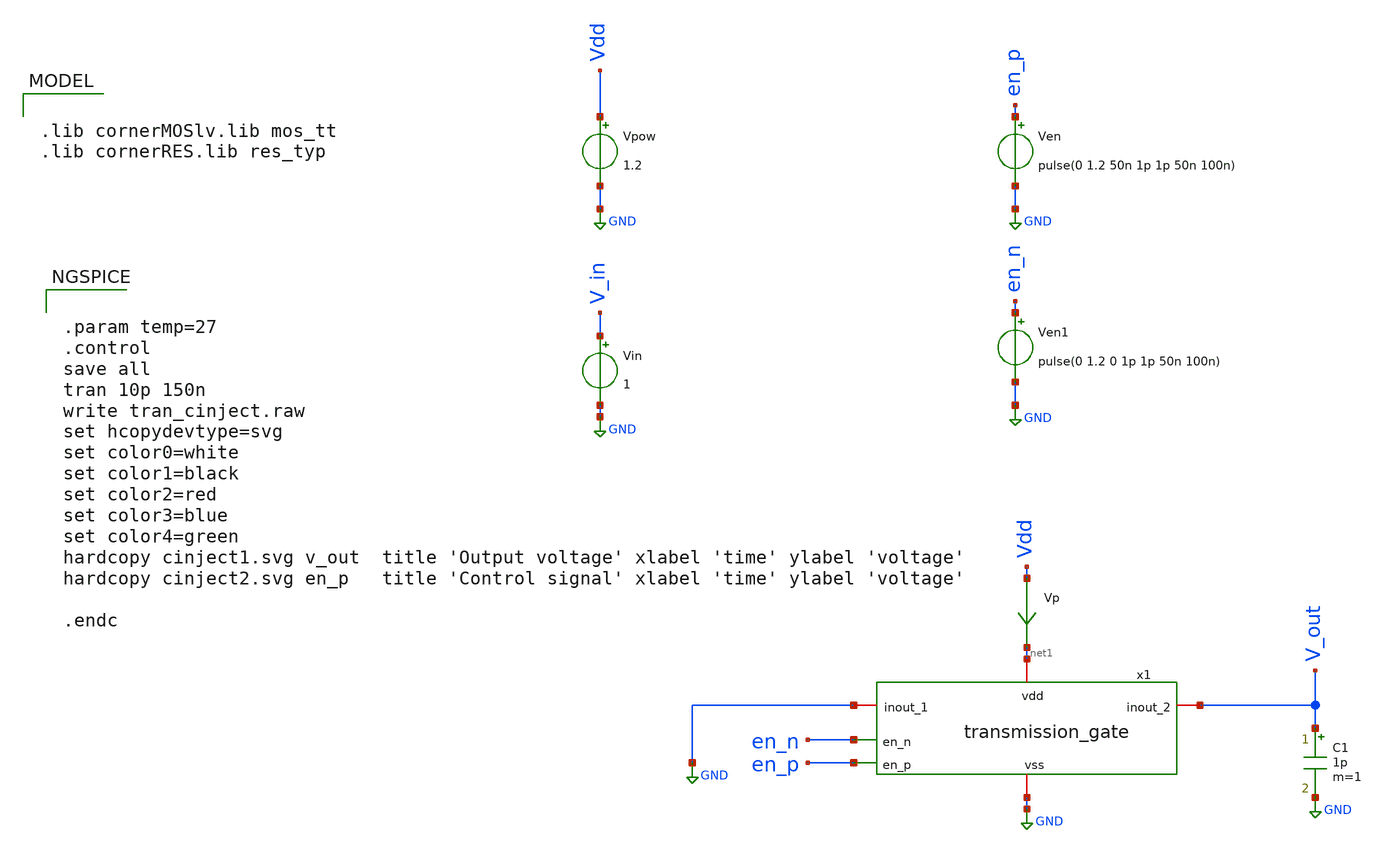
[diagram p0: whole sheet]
** sch_path: CHIPCHILE_CANELOS24_WorkshopTO/design_data/xschem/tgate/transmission_gate_tb_Cinject.sch
* Copyright 2023 IHP PDK Authors
**.subckt transmission_gate_tb_Cinject
Vpow Vdd GND 1.2
Vp Vdd net1 0
.save i(vp)
Vin V_in GND 1
Ven en_p GND pulse(0 1.2 50n 1p 1p 50n 100n)
C1 V_out GND 1p m=1
Ven1 en_n GND pulse(0 1.2 0 1p 1p 50n 100n)
x1 net1 en_n GND V_out en_p GND transmission_gate
**** begin user architecture code

.lib cornerMOSlv.lib mos_tt
.lib cornerRES.lib res_typ



.param temp=27
.control
save all
tran 10p 150n
write tran_cinject.raw
set hcopydevtype=svg
set color0=white
set color1=black
set color2=red
set color3=blue
set color4=green
hardcopy cinject1.svg v_out  title 'Output voltage' xlabel 'time' ylabel 'voltage'
hardcopy cinject2.svg en_p   title 'Control signal' xlabel 'time' ylabel 'voltage'

.endc


**** end user architecture code
**.ends

* expanding   symbol:  transmission_gate.sym # of pins=6
** sym_path: CHIPCHILE_CANELOS24_WorkshopTO/design_data/xschem/multiplexer/transmission_gate.sym
** sch_path: CHIPCHILE_CANELOS24_WorkshopTO/design_data/xschem/multiplexer/transmission_gate.sch
.subckt transmission_gate vdd en_n inout_1 inout_2 en_p vss
*.iopin inout_1
*.iopin inout_2
*.ipin en_p
*.iopin vdd
*.iopin vss
*.ipin en_n
XM1 inout_1 en_p inout_2 net1 sg13_lv_nmos w=200.0u l=0.130u ng=20 m=1 mm_ok=1
XM2 inout_1 en_n inout_2 net2 sg13_lv_pmos w=200.0u l=0.130u ng=20 m=1 mm_ok=1
XR1 vdd net2 ntap1 R=262.8 w=0.78e-6 l=0.78e-6
XR2 vss net1 ptap1 R=262.8 w=0.78e-6 l=0.78e-6
.ends

.GLOBAL GND
.end
